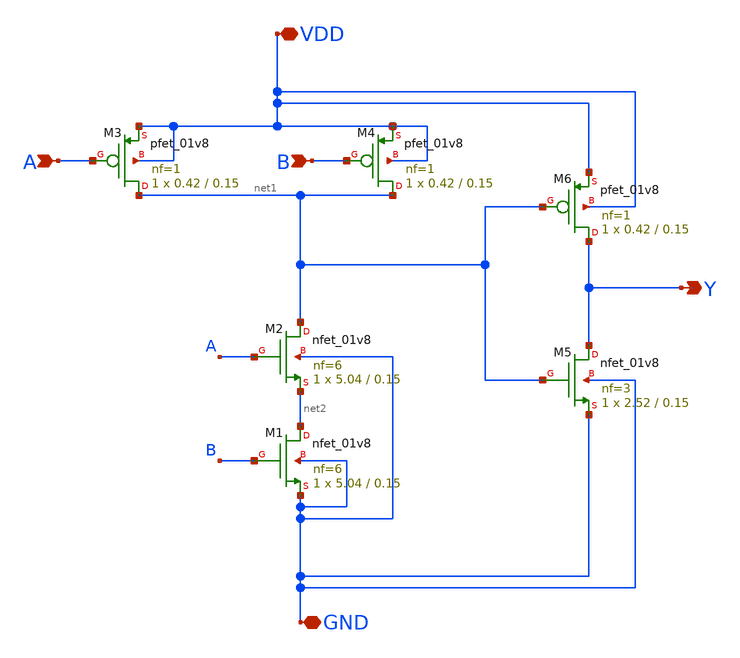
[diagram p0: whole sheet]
** sch_path: cells/AND2X1/schematic/and2x1.sch
**.subckt and2x1 A B VDD GND Y
*.ipin A
*.ipin B
*.iopin VDD
*.iopin GND
*.opin Y
XM2 net1 A net2 GND sky130_fd_pr__nfet_01v8 L=0.15 W=5.04 nf=6 ad='int((6 + 1)/2) * 5.04 / 6 * 0.29'
+ as='int((6 + 2)/2) * 5.04 / 6 * 0.29' pd='2*int((6 + 1)/2) * (5.04 / 6 + 0.29)' ps='2*int((6 + 2)/2) * (5.04 / 6 + 0.29)'
+ nrd='0.29 / 5.04 ' nrs='0.29 / 5.04 ' sa=0 sb=0 sd=0 mult=1 m=1
XM3 net1 A VDD VDD sky130_fd_pr__pfet_01v8 L=0.15 W=0.42 nf=1 ad='int((1 + 1)/2) * 0.42 / 1 * 0.29' as='int((1 + 2)/2) * 0.42 / 1 * 0.29'
+ pd='2*int((1 + 1)/2) * (0.42 / 1 + 0.29)' ps='2*int((1 + 2)/2) * (0.42 / 1 + 0.29)' nrd='0.29 / 0.42 '
+ nrs='0.29 / 0.42 ' sa=0 sb=0 sd=0 mult=1 m=1
XM5 Y net1 GND GND sky130_fd_pr__nfet_01v8 L=0.15 W=2.52 nf=3 ad='int((3 + 1)/2) * 2.52 / 3 * 0.29' as='int((3 + 2)/2) * 2.52 / 3 * 0.29'
+ pd='2*int((3 + 1)/2) * (2.52 / 3 + 0.29)' ps='2*int((3 + 2)/2) * (2.52 / 3 + 0.29)' nrd='0.29 / 2.52 '
+ nrs='0.29 / 2.52 ' sa=0 sb=0 sd=0 mult=1 m=1
XM4 net1 B VDD VDD sky130_fd_pr__pfet_01v8 L=0.15 W=0.42 nf=1 ad='int((1 + 1)/2) * 0.42 / 1 * 0.29' as='int((1 + 2)/2) * 0.42 / 1 * 0.29'
+ pd='2*int((1 + 1)/2) * (0.42 / 1 + 0.29)' ps='2*int((1 + 2)/2) * (0.42 / 1 + 0.29)' nrd='0.29 / 0.42 '
+ nrs='0.29 / 0.42 ' sa=0 sb=0 sd=0 mult=1 m=1
XM6 Y net1 VDD VDD sky130_fd_pr__pfet_01v8 L=0.15 W=0.42 nf=1 ad='int((1 + 1)/2) * 0.42 / 1 * 0.29' as='int((1 + 2)/2) * 0.42 / 1 * 0.29'
+ pd='2*int((1 + 1)/2) * (0.42 / 1 + 0.29)' ps='2*int((1 + 2)/2) * (0.42 / 1 + 0.29)' nrd='0.29 / 0.42 '
+ nrs='0.29 / 0.42 ' sa=0 sb=0 sd=0 mult=1 m=1
XM1 net2 B GND GND sky130_fd_pr__nfet_01v8 L=0.15 W=5.04 nf=6 ad='int((6 + 1)/2) * 5.04 / 6 * 0.29' as='int((6 + 2)/2) * 5.04 / 6 * 0.29'
+ pd='2*int((6 + 1)/2) * (5.04 / 6 + 0.29)' ps='2*int((6 + 2)/2) * (5.04 / 6 + 0.29)' nrd='0.29 / 5.04 '
+ nrs='0.29 / 5.04 ' sa=0 sb=0 sd=0 mult=1 m=1
**.ends
.end
